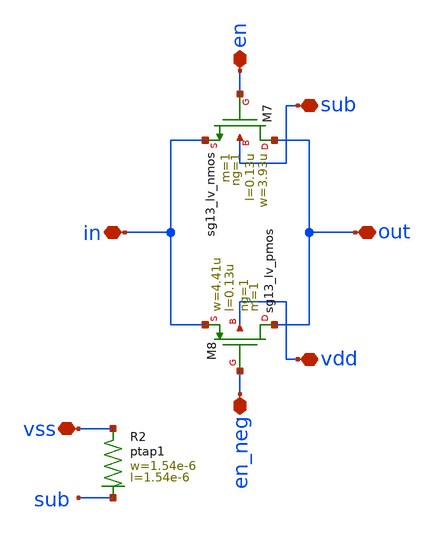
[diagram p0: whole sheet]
** sch_path: ihp-sg13g2/libs.tech/xschem/hm_stdcells/hm_Tgate_noptap.sch
**.subckt hm_Tgate_noptap sub vdd en in out en_neg vss
*.iopin sub
*.iopin vdd
*.iopin en
*.iopin in
*.iopin out
*.iopin en_neg
*.iopin vss
XM7 out en in sub sg13_lv_nmos w=3.93u l=0.13u ng=1 m=1 mm_ok=1
XM8 out en_neg in vdd sg13_lv_pmos w=4.41u l=0.13u ng=1 m=1 mm_ok=1
XR2 vss sub ptap1 R=114.9 w=1.54e-6 l=1.54e-6
**.ends
.end
